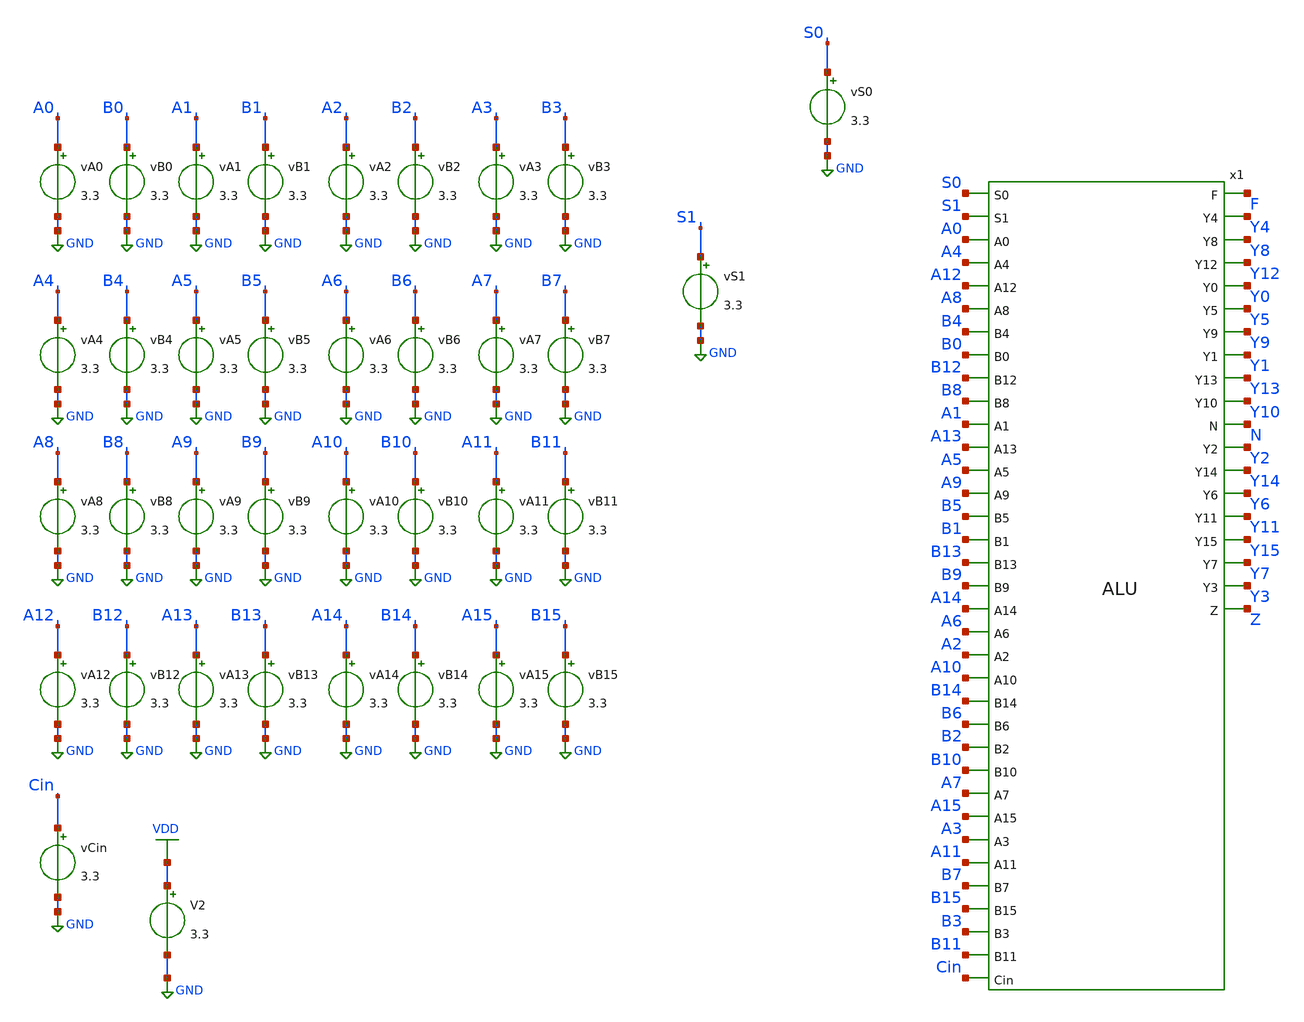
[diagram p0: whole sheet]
** sch_path: tbs/alu_tb_cmpne.sch
**.subckt alu_tb_cmpne
x1 S0 S1 F A0 A4 A12 A8 B4 B0 B12 B8 A1 A13 A5 A9 Y4 Y8 Y12 Y0 B5 B1 B13 B9 Y5 Y9 Y1 Y13 A14 A6 A2
+ A10 Y10 N Y2 Y14 Y6 B14 B6 B2 B10 Y11 Y15 Y7 Y3 A7 A15 A3 A11 B7 B15 B3 B11 Cin Z ALU
vA0 A0 GND 3.3
vB0 B0 GND 3.3
vA1 A1 GND 3.3
vB1 B1 GND 3.3
vA2 A2 GND 3.3
vB2 B2 GND 3.3
vA3 A3 GND 3.3
vB3 B3 GND 3.3
vA4 A4 GND 3.3
vB4 B4 GND 3.3
vA5 A5 GND 3.3
vB5 B5 GND 3.3
vA6 A6 GND 3.3
vB6 B6 GND 3.3
vA7 A7 GND 3.3
vB7 B7 GND 3.3
vA8 A8 GND 3.3
vB8 B8 GND 3.3
vA9 A9 GND 3.3
vB9 B9 GND 3.3
vA10 A10 GND 3.3
vB10 B10 GND 3.3
vA11 A11 GND 3.3
vB11 B11 GND 3.3
vA12 A12 GND 3.3
vB12 B12 GND 3.3
vA13 A13 GND 3.3
vB13 B13 GND 3.3
vA14 A14 GND 3.3
vB14 B14 GND 3.3
vA15 A15 GND 3.3
vB15 B15 GND 3.3
vS0 S0 GND 3.3
vS1 S1 GND 3.3
vCin Cin GND 3.3
V2 VDD GND 3.3
**** begin user architecture code


.control
  let vlow = 0
  let vhigh = 3.3

  * CMP mode assumed as ADD path with Cin=1
  alter VS1 = $&vlow
  alter VS0 = $&vlow
  alter VCin = $&vhigh

  * A = 0x0003
  alter VA15 = $&vlow
  alter VA14 = $&vlow
  alter VA13 = $&vlow
  alter VA12 = $&vlow
  alter VA11 = $&vlow
  alter VA10 = $&vlow
  alter VA9  = $&vlow
  alter VA8  = $&vlow
  alter VA7  = $&vlow
  alter VA6  = $&vlow
  alter VA5  = $&vlow
  alter VA4  = $&vlow
  alter VA3  = $&vlow
  alter VA2  = $&vlow
  alter VA1  = $&vhigh
  alter VA0  = $&vhigh

  * B = 0x0005
  alter VB15 = $&vlow
  alter VB14 = $&vlow
  alter VB13 = $&vlow
  alter VB12 = $&vlow
  alter VB11 = $&vlow
  alter VB10 = $&vlow
  alter VB9  = $&vlow
  alter VB8  = $&vlow
  alter VB7  = $&vlow
  alter VB6  = $&vlow
  alter VB5  = $&vlow
  alter VB4  = $&vlow
  alter VB3  = $&vlow
  alter VB2  = $&vhigh
  alter VB1  = $&vlow
  alter VB0  = $&vhigh

  op
  echo EXPECTED: Z=0, N=1
  print v(z) v(n) v(f)

  tran 0.1n 30n
  meas tran vz find v(z) at=30n
  meas tran vn find v(n) at=30n
  meas tran vf find v(f) at=30n

  print vz vn vf
  write alu_cmp_notequal_results.raw
.endc



.include $::180MCU_MODELS/design.ngspice
.lib $::180MCU_MODELS/sm141064.ngspice typical

**** end user architecture code
**.ends
.GLOBAL GND
.GLOBAL VDD
.end
